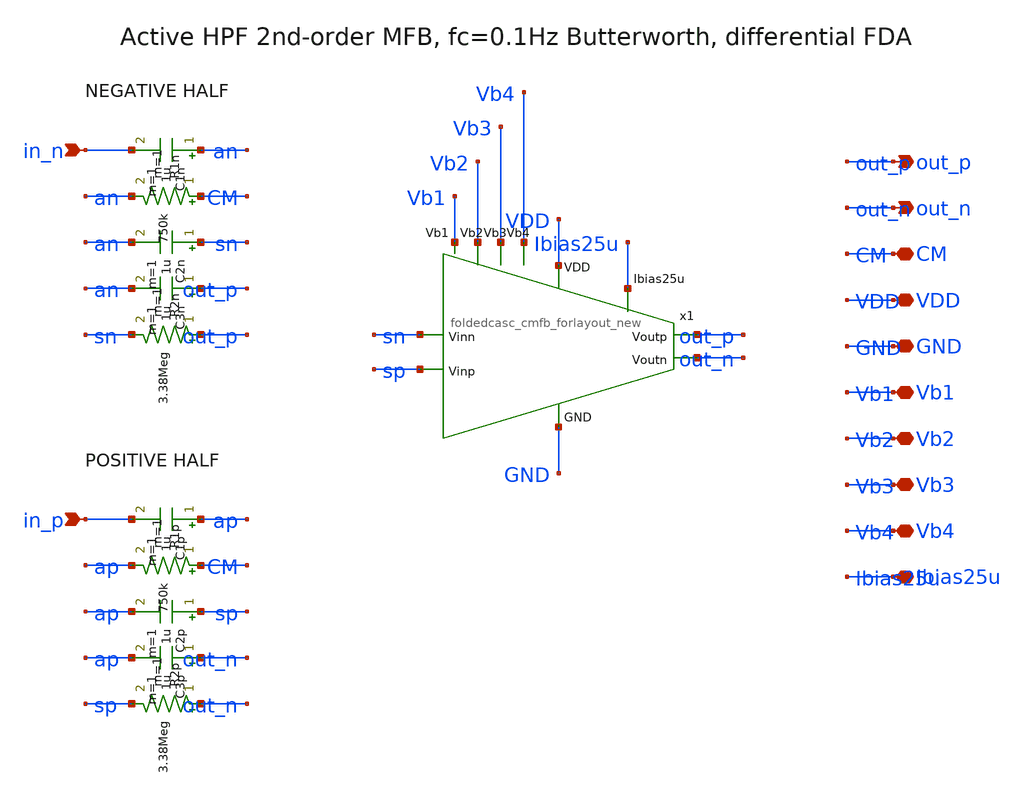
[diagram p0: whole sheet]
** sch_path: ps-filters/hpf.sch
**.subckt hpf in_p in_n out_p out_n CM VDD GND Vb1 Vb2 Vb3 Vb4 Ibias25u
*.ipin in_p
*.ipin in_n
*.opin out_p
*.opin out_n
*.iopin CM
*.iopin VDD
*.iopin GND
*.iopin Vb1
*.iopin Vb2
*.iopin Vb3
*.iopin Vb4
*.iopin Ibias25u
C1p ap in_p 1u m=1
R1p CM ap 750k m=1
C2p sp ap 1u m=1
C3p out_n ap 1u m=1
R2p out_n sp 3.38Meg m=1
C1n an in_n 1u m=1
R1n CM an 750k m=1
C2n sn an 1u m=1
C3n out_p an 1u m=1
R2n out_p sn 3.38Meg m=1
x1 VDD Vb2 out_p out_n Vb1 Ibias25u sn GND sp Vb3 Vb4 foldedcasc_cmfb_forlayout_new
**.ends

* expanding   symbol:  chipathon-2026-ppg/jz_fda2/xschem/foldedcasc_cmfb_forlayout_new.sym # of
*+ pins=11
** sym_path: jz_fda2/xschem/foldedcasc_cmfb_forlayout_new.sym
** sch_path: jz_fda2/xschem/foldedcasc_cmfb_forlayout_new.sch
.subckt foldedcasc_cmfb_forlayout_new VDD Vb2 Voutp Voutn Vb1 Ibias25u Vinn GND Vinp Vb3 Vb4
*.ipin VDD
*.opin Voutp
*.ipin Vinn
*.ipin Ibias25u
*.ipin GND
*.ipin Vinp
*.opin Voutn
*.ipin Vb4
*.ipin Vb1
*.ipin Vb2
*.ipin Vb3
XM5 net1 Vb3 GND GND nfet_03v3 L=0.56u W=26u nf=4 ad='int((nf+1)/2) * W/nf * 0.18u' as='int((nf+2)/2) * W/nf * 0.18u'
+ pd='2*int((nf+1)/2) * (W/nf + 0.18u)' ps='2*int((nf+2)/2) * (W/nf + 0.18u)' nrd='0.18u / W' nrs='0.18u / W'
+ sa=0 sb=0 sd=0 m=1
XM6 Voutn Vb2 net2 GND nfet_03v3 L=0.56u W=35u nf=2 ad='int((nf+1)/2) * W/nf * 0.18u' as='int((nf+2)/2) * W/nf * 0.18u'
+ pd='2*int((nf+1)/2) * (W/nf + 0.18u)' ps='2*int((nf+2)/2) * (W/nf + 0.18u)' nrd='0.18u / W' nrs='0.18u / W'
+ sa=0 sb=0 sd=0 m=1
XM7 Voutp Vb2 net1 GND nfet_03v3 L=0.56u W=35u nf=2 ad='int((nf+1)/2) * W/nf * 0.18u' as='int((nf+2)/2) * W/nf * 0.18u'
+ pd='2*int((nf+1)/2) * (W/nf + 0.18u)' ps='2*int((nf+2)/2) * (W/nf + 0.18u)' nrd='0.18u / W' nrs='0.18u / W'
+ sa=0 sb=0 sd=0 m=1
XM8 Voutn Vb1 net3 VDD pfet_03v3 L=0.56u W=24u nf=5 ad='int((nf+1)/2) * W/nf * 0.18u' as='int((nf+2)/2) * W/nf * 0.18u'
+ pd='2*int((nf+1)/2) * (W/nf + 0.18u)' ps='2*int((nf+2)/2) * (W/nf + 0.18u)' nrd='0.18u / W' nrs='0.18u / W'
+ sa=0 sb=0 sd=0 m=1
XM9 Voutp Vb1 net4 VDD pfet_03v3 L=0.56u W=24u nf=5 ad='int((nf+1)/2) * W/nf * 0.18u' as='int((nf+2)/2) * W/nf * 0.18u'
+ pd='2*int((nf+1)/2) * (W/nf + 0.18u)' ps='2*int((nf+2)/2) * (W/nf + 0.18u)' nrd='0.18u / W' nrs='0.18u / W'
+ sa=0 sb=0 sd=0 m=1
XM10 net3 Vb4 VDD VDD pfet_03v3 L=0.56u W=23u nf=4 ad='int((nf+1)/2) * W/nf * 0.18u' as='int((nf+2)/2) * W/nf * 0.18u'
+ pd='2*int((nf+1)/2) * (W/nf + 0.18u)' ps='2*int((nf+2)/2) * (W/nf + 0.18u)' nrd='0.18u / W' nrs='0.18u / W'
+ sa=0 sb=0 sd=0 m=1
XM11 net4 Vb4 VDD VDD pfet_03v3 L=0.56u W=23u nf=4 ad='int((nf+1)/2) * W/nf * 0.18u' as='int((nf+2)/2) * W/nf * 0.18u'
+ pd='2*int((nf+1)/2) * (W/nf + 0.18u)' ps='2*int((nf+2)/2) * (W/nf + 0.18u)' nrd='0.18u / W' nrs='0.18u / W'
+ sa=0 sb=0 sd=0 m=1
XM1 net1 Vinn net5 VDD pfet_03v3 L=0.28u W=3.45u nf=1 ad='int((nf+1)/2) * W/nf * 0.18u' as='int((nf+2)/2) * W/nf * 0.18u'
+ pd='2*int((nf+1)/2) * (W/nf + 0.18u)' ps='2*int((nf+2)/2) * (W/nf + 0.18u)' nrd='0.18u / W' nrs='0.18u / W'
+ sa=0 sb=0 sd=0 m=1
XM2 net2 Vinp net5 VDD pfet_03v3 L=0.28u W=3.45u nf=1 ad='int((nf+1)/2) * W/nf * 0.18u' as='int((nf+2)/2) * W/nf * 0.18u'
+ pd='2*int((nf+1)/2) * (W/nf + 0.18u)' ps='2*int((nf+2)/2) * (W/nf + 0.18u)' nrd='0.18u / W' nrs='0.18u / W'
+ sa=0 sb=0 sd=0 m=1
XM3 net5 Ibias25u net6 VDD pfet_03v3 L=0.28u W=4.9u nf=2 ad='int((nf+1)/2) * W/nf * 0.18u' as='int((nf+2)/2) * W/nf * 0.18u'
+ pd='2*int((nf+1)/2) * (W/nf + 0.18u)' ps='2*int((nf+2)/2) * (W/nf + 0.18u)' nrd='0.18u / W' nrs='0.18u / W'
+ sa=0 sb=0 sd=0 m=1
XM12 Ibias25u Ibias25u VDD VDD pfet_03v3 L=0.28u W=2.27u nf=1 ad='int((nf+1)/2) * W/nf * 0.18u' as='int((nf+2)/2) * W/nf * 0.18u'
+ pd='2*int((nf+1)/2) * (W/nf + 0.18u)' ps='2*int((nf+2)/2) * (W/nf + 0.18u)' nrd='0.18u / W' nrs='0.18u / W'
+ sa=0 sb=0 sd=0 m=1
XM13 net6 Voutp VDD VDD pfet_03v3 L=0.28u W=30u nf=3 ad='int((nf+1)/2) * W/nf * 0.18u' as='int((nf+2)/2) * W/nf * 0.18u'
+ pd='2*int((nf+1)/2) * (W/nf + 0.18u)' ps='2*int((nf+2)/2) * (W/nf + 0.18u)' nrd='0.18u / W' nrs='0.18u / W'
+ sa=0 sb=0 sd=0 m=1
XM14 net6 Voutn VDD VDD pfet_03v3 L=0.28u W=30u nf=3 ad='int((nf+1)/2) * W/nf * 0.18u' as='int((nf+2)/2) * W/nf * 0.18u'
+ pd='2*int((nf+1)/2) * (W/nf + 0.18u)' ps='2*int((nf+2)/2) * (W/nf + 0.18u)' nrd='0.18u / W' nrs='0.18u / W'
+ sa=0 sb=0 sd=0 m=1
XM4 net2 Vb3 GND GND nfet_03v3 L=0.56u W=26u nf=4 ad='int((nf+1)/2) * W/nf * 0.18u' as='int((nf+2)/2) * W/nf * 0.18u'
+ pd='2*int((nf+1)/2) * (W/nf + 0.18u)' ps='2*int((nf+2)/2) * (W/nf + 0.18u)' nrd='0.18u / W' nrs='0.18u / W'
+ sa=0 sb=0 sd=0 m=1
XM15 VDD VDD VDD VDD pfet_03v3 L=0.28u W=2.27u nf=1 ad='int((nf+1)/2) * W/nf * 0.18u' as='int((nf+2)/2) * W/nf * 0.18u'
+ pd='2*int((nf+1)/2) * (W/nf + 0.18u)' ps='2*int((nf+2)/2) * (W/nf + 0.18u)' nrd='0.18u / W' nrs='0.18u / W'
+ sa=0 sb=0 sd=0 m=1
.ends

.end
